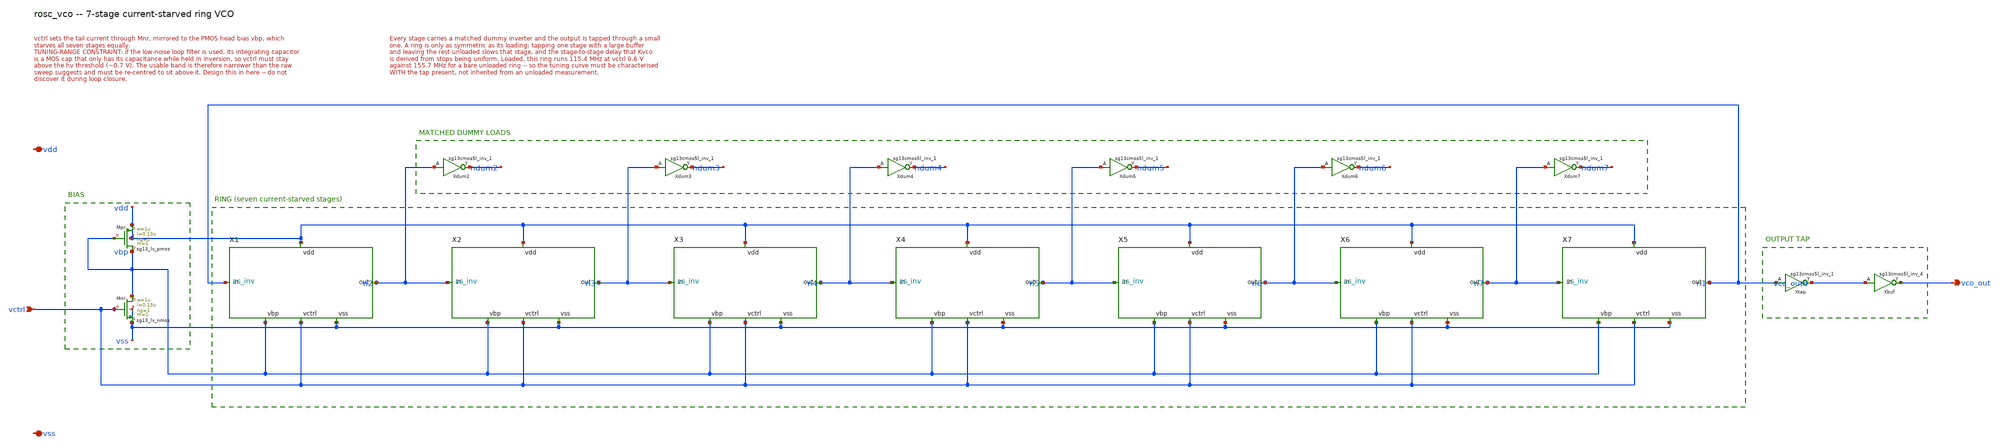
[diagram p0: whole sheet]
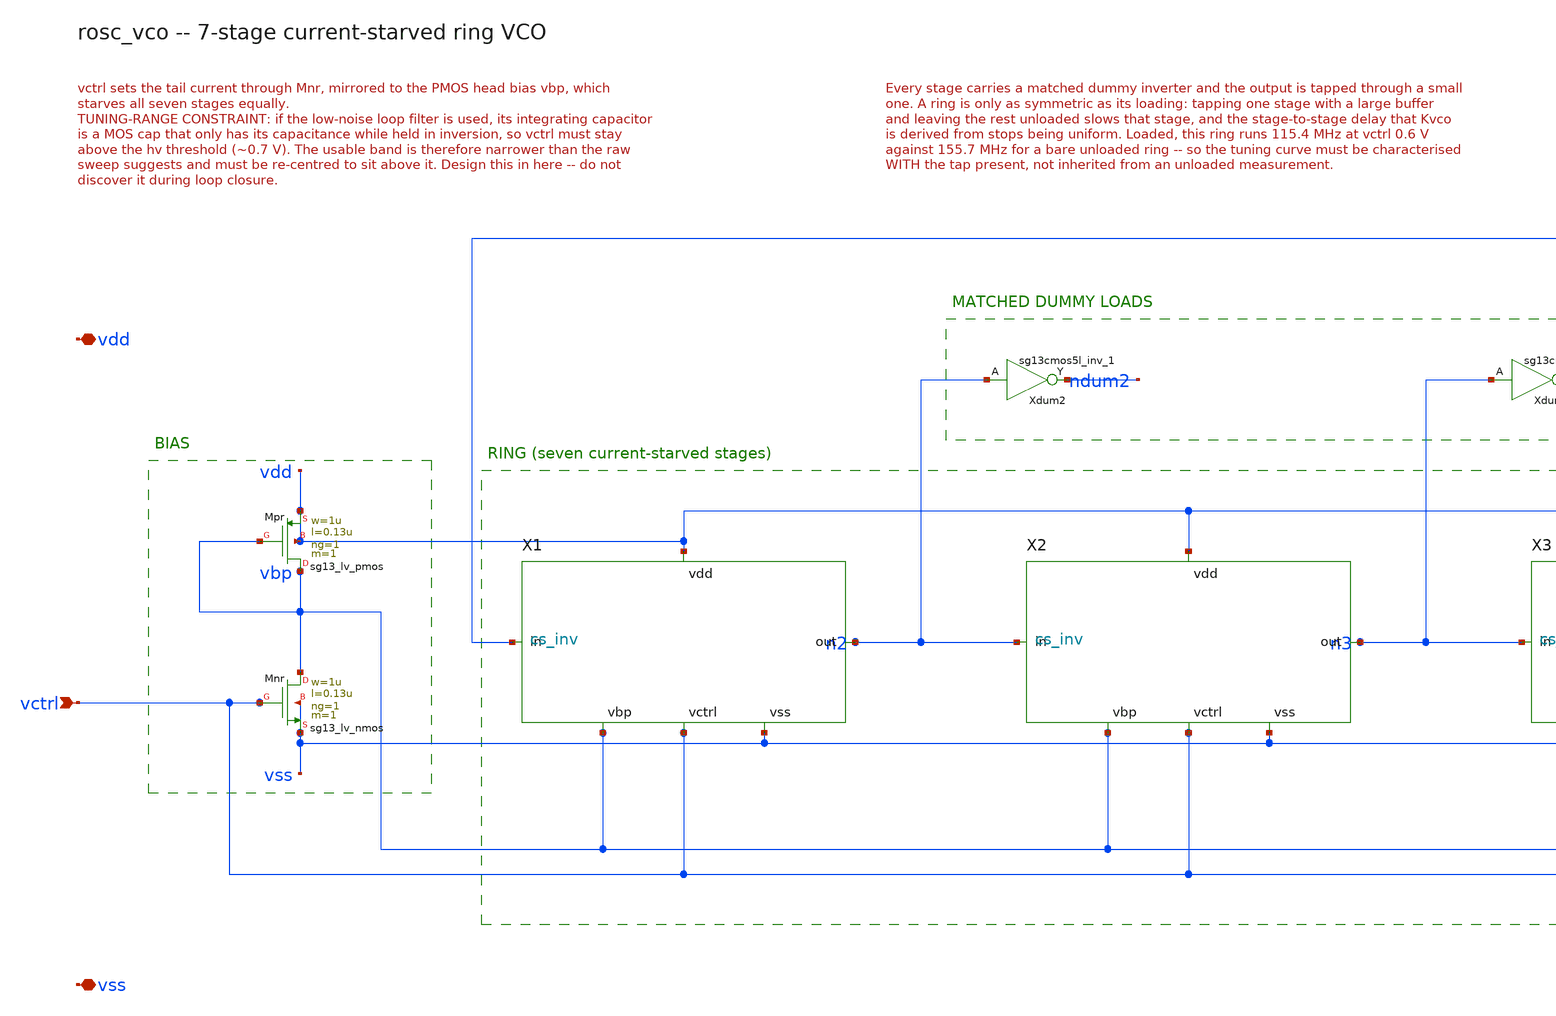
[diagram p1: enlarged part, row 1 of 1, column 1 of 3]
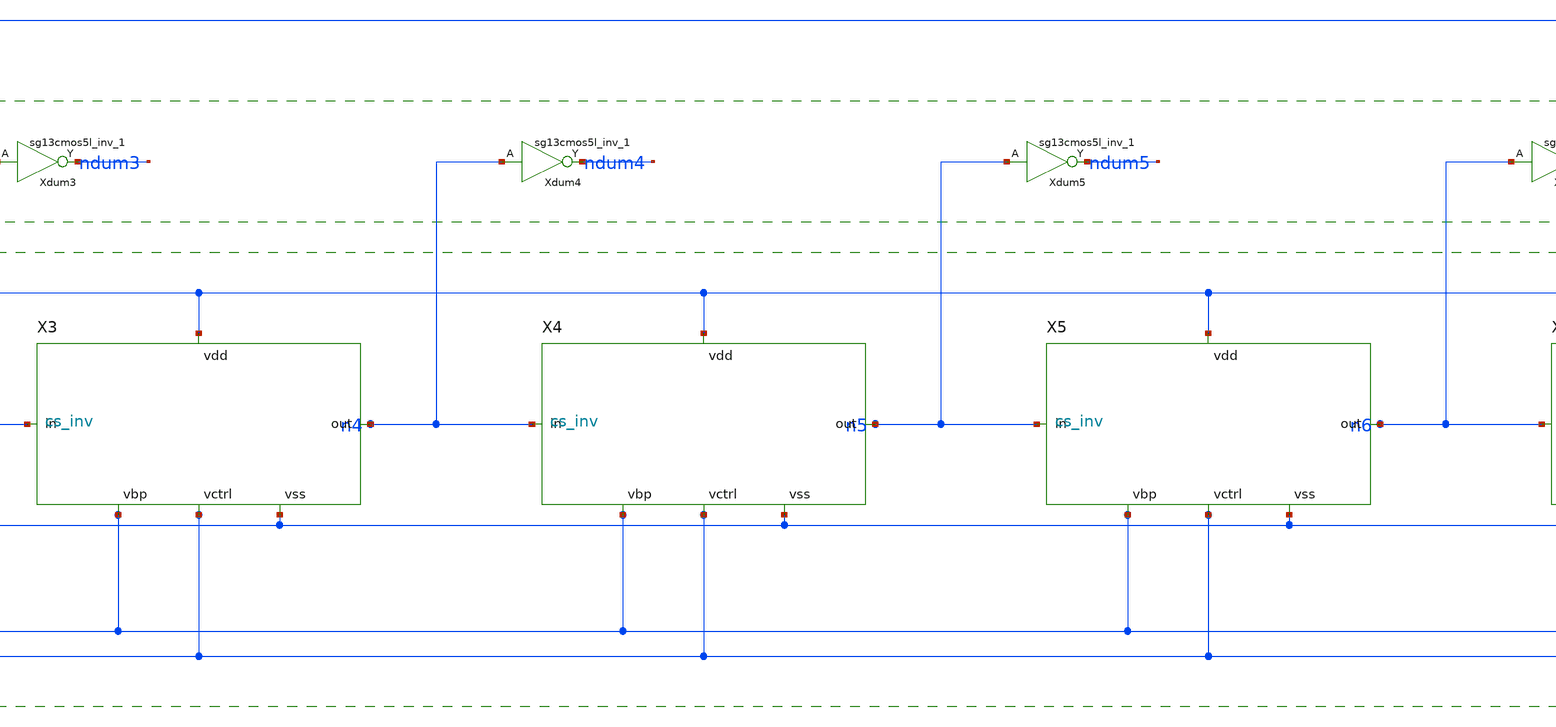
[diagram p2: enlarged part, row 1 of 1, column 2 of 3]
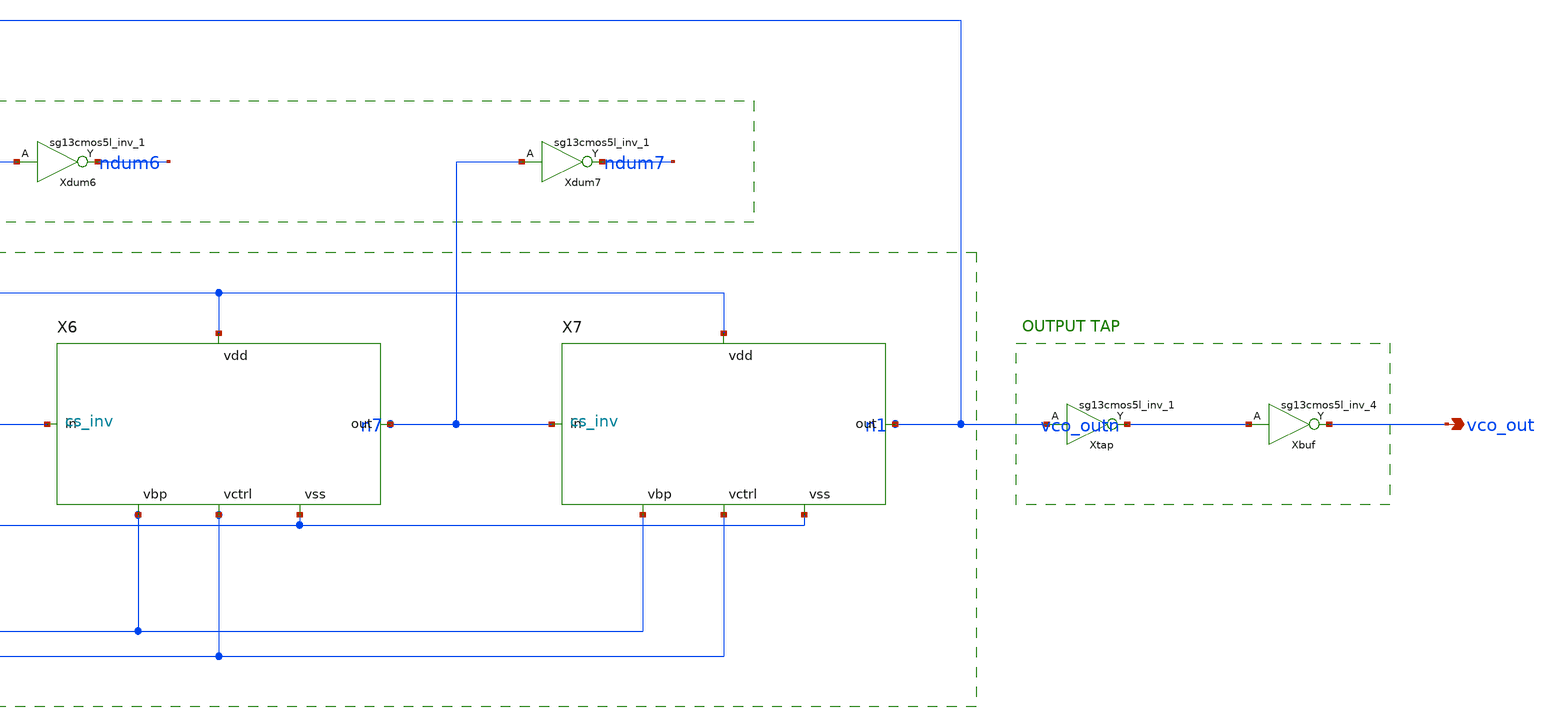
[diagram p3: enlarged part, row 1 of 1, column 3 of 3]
** sch_path: xschem/rosc_vco_wired.sch
**.subckt rosc_vco_wired vctrl vco_out vdd vss
*.ipin vctrl
*.opin vco_out
*.iopin vdd
*.iopin vss
XMpr vbp vbp vdd vdd sg13_lv_pmos w=1u l=0.13u ng=1 m=1 mm_ok=1
XMnr vbp vctrl vss vss sg13_lv_nmos w=1u l=0.13u ng=1 m=1 mm_ok=1
X1 n1 n2 vdd vbp vctrl vss cs_inv
X2 n2 n3 vdd vbp vctrl vss cs_inv
X3 n3 n4 vdd vbp vctrl vss cs_inv
X4 n4 n5 vdd vbp vctrl vss cs_inv
X5 n5 n6 vdd vbp vctrl vss cs_inv
X6 n6 n7 vdd vbp vctrl vss cs_inv
X7 n7 n1 vdd vbp vctrl vss cs_inv
Xtap vco_outn n1 vdd vss sg13cmos5l_inv_1
Xbuf vco_out vco_outn vdd vss sg13cmos5l_inv_4
Xdum2 ndum2 n2 vdd vss sg13cmos5l_inv_1
Xdum3 ndum3 n3 vdd vss sg13cmos5l_inv_1
Xdum4 ndum4 n4 vdd vss sg13cmos5l_inv_1
Xdum5 ndum5 n5 vdd vss sg13cmos5l_inv_1
Xdum6 ndum6 n6 vdd vss sg13cmos5l_inv_1
Xdum7 ndum7 n7 vdd vss sg13cmos5l_inv_1
**.ends

* expanding   symbol:  cs_inv.sym # of pins=6
** sym_path: xschem/cs_inv.sym
** sch_path: xschem/cs_inv.sch
.subckt cs_inv in out vdd vbp vctrl vss
*.ipin in
*.opin out
*.ipin vbp
*.ipin vctrl
*.iopin vdd
*.iopin vss
XMps nph vbp vdd vdd sg13_lv_pmos w=1u l=0.13u ng=1 m=1 mm_ok=1
XMpu out in nph vdd sg13_lv_pmos w=2u l=0.13u ng=1 m=1 mm_ok=1
XMnd out in npl vss sg13_lv_nmos w=2u l=0.13u ng=1 m=1 mm_ok=1
XMns npl vctrl vss vss sg13_lv_nmos w=1u l=0.13u ng=1 m=1 mm_ok=1
.ends

.end
